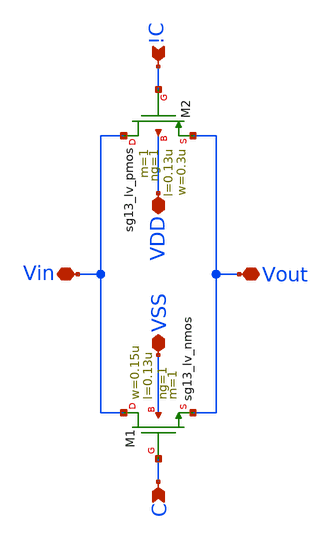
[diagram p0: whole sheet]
** sch_path: xschem/t_gate.sch
**.subckt t_gate VSS VDD Vout Vin C !C
*.iopin VSS
*.iopin VDD
*.iopin Vout
*.iopin Vin
*.ipin C
*.ipin !C
XM1 Vin C Vout VSS sg13_lv_nmos w=0.15u l=0.13u ng=1 m=1 mm_ok=1
XM2 Vin !C Vout VDD sg13_lv_pmos w=0.3u l=0.13u ng=1 m=1 mm_ok=1
**.ends
.end
